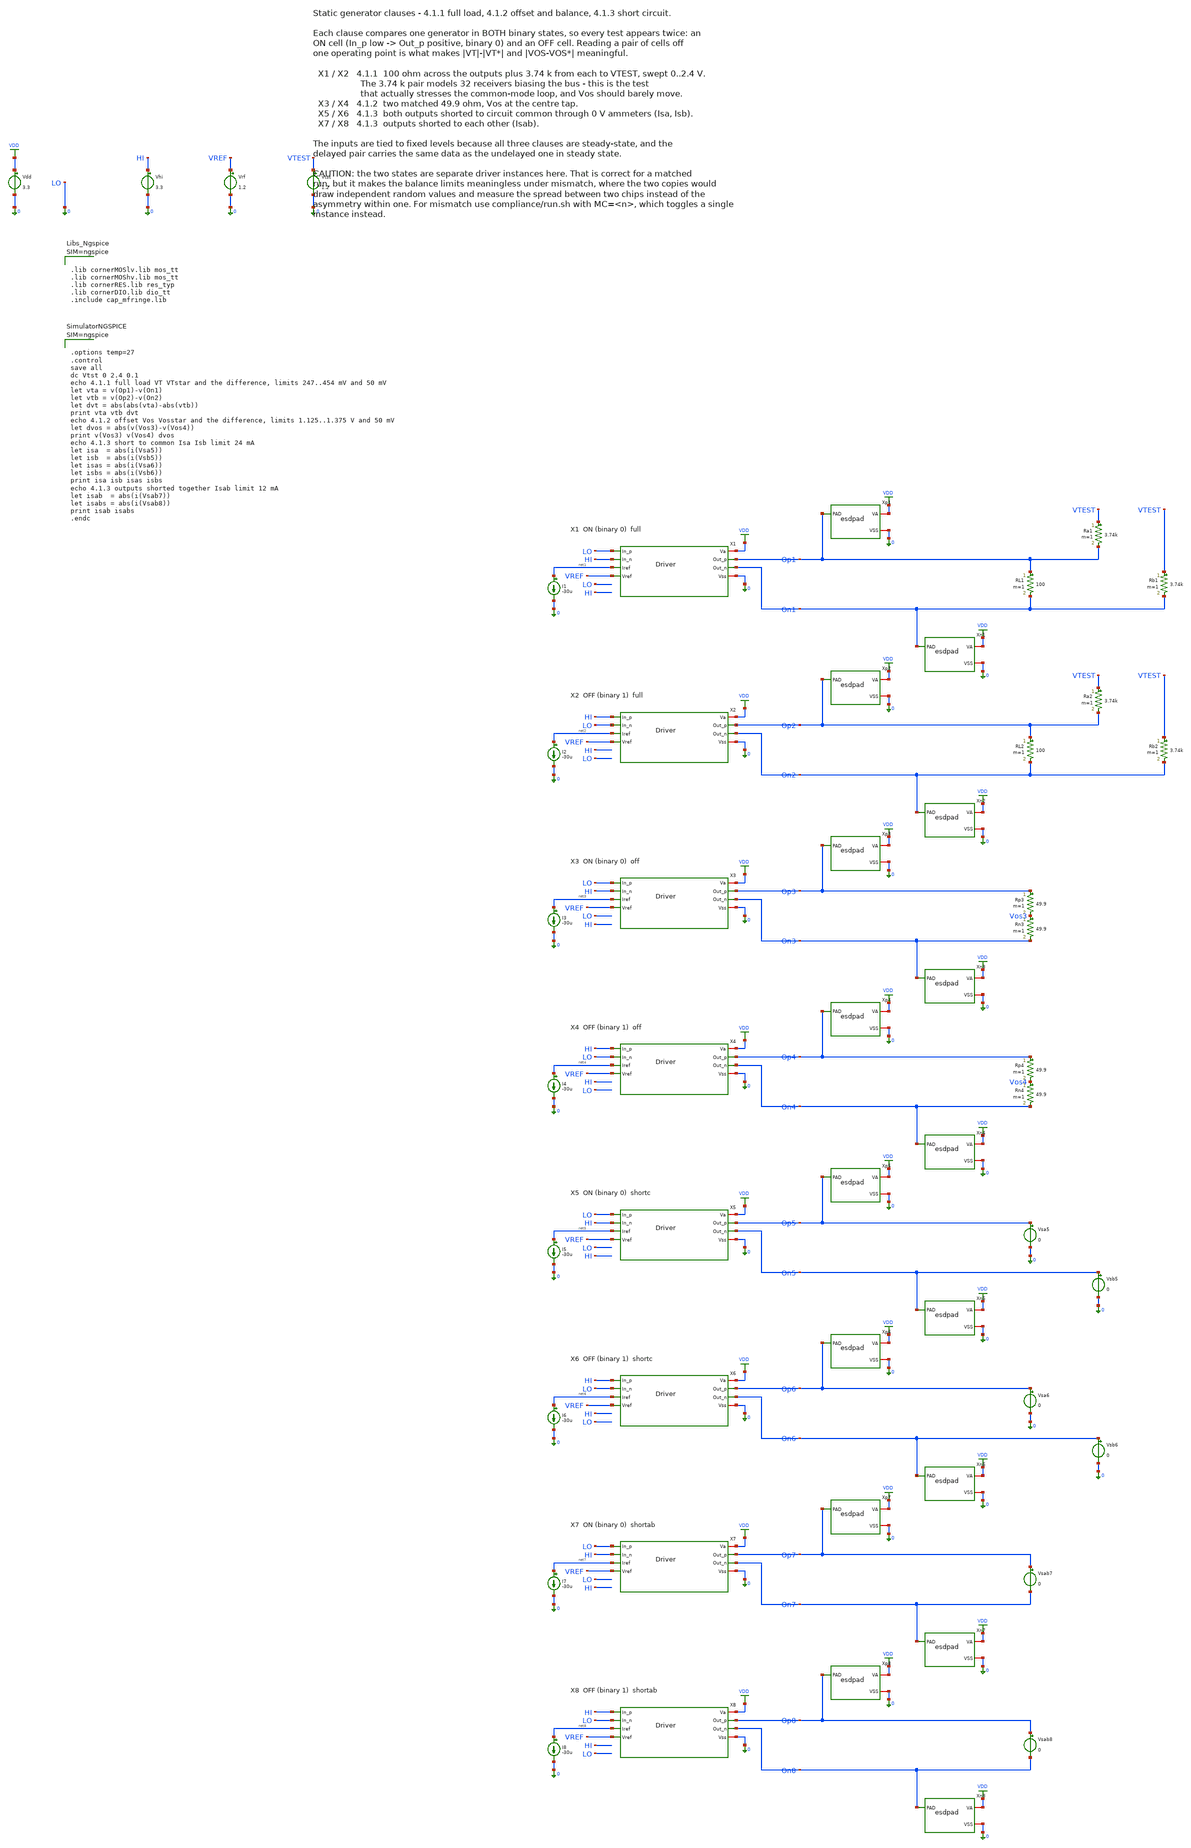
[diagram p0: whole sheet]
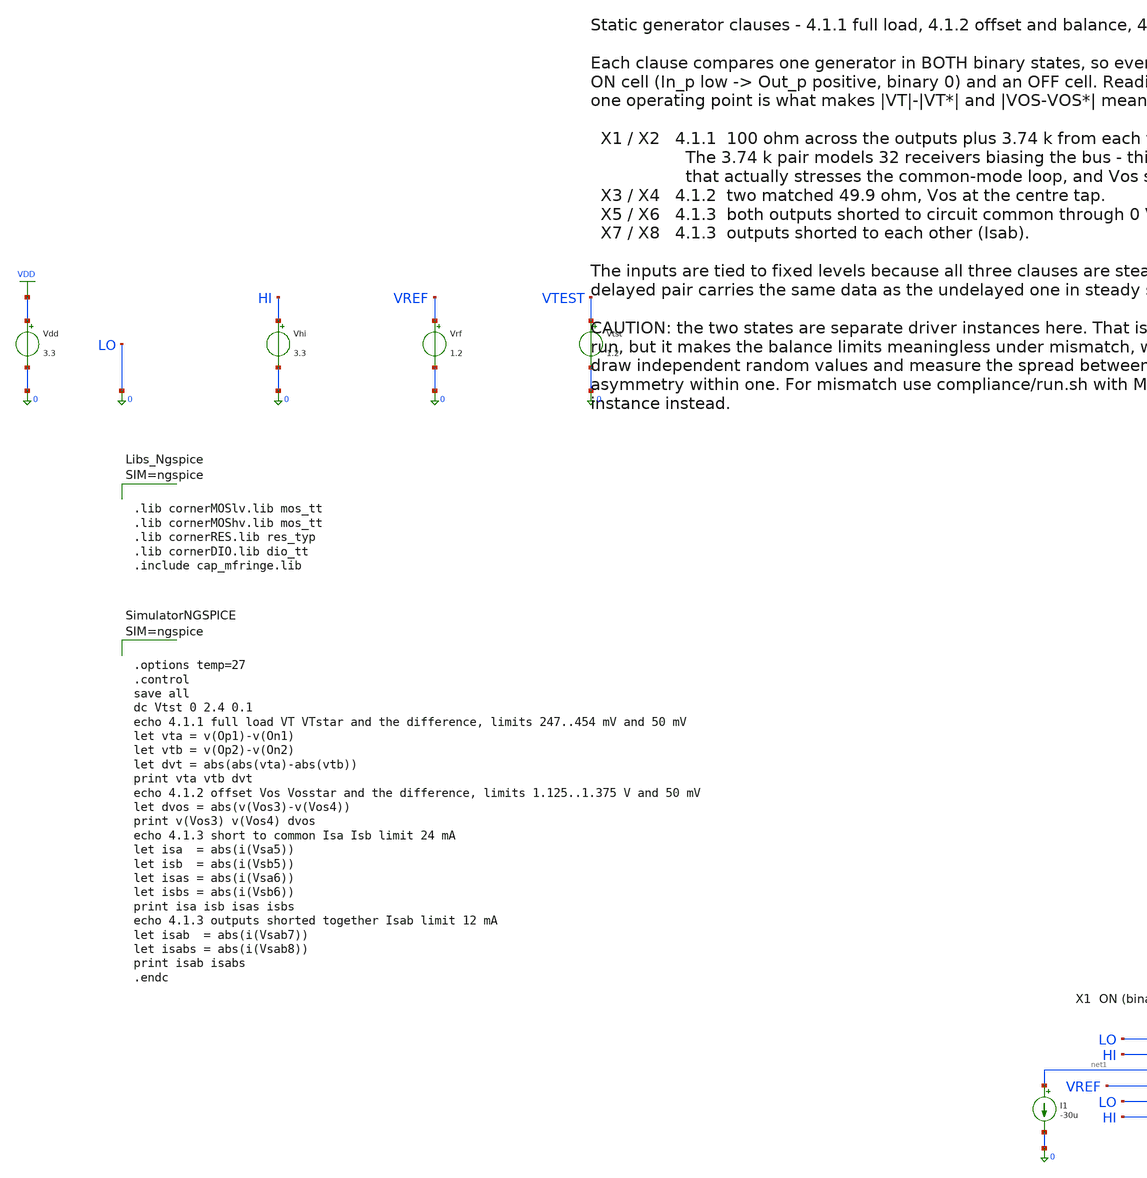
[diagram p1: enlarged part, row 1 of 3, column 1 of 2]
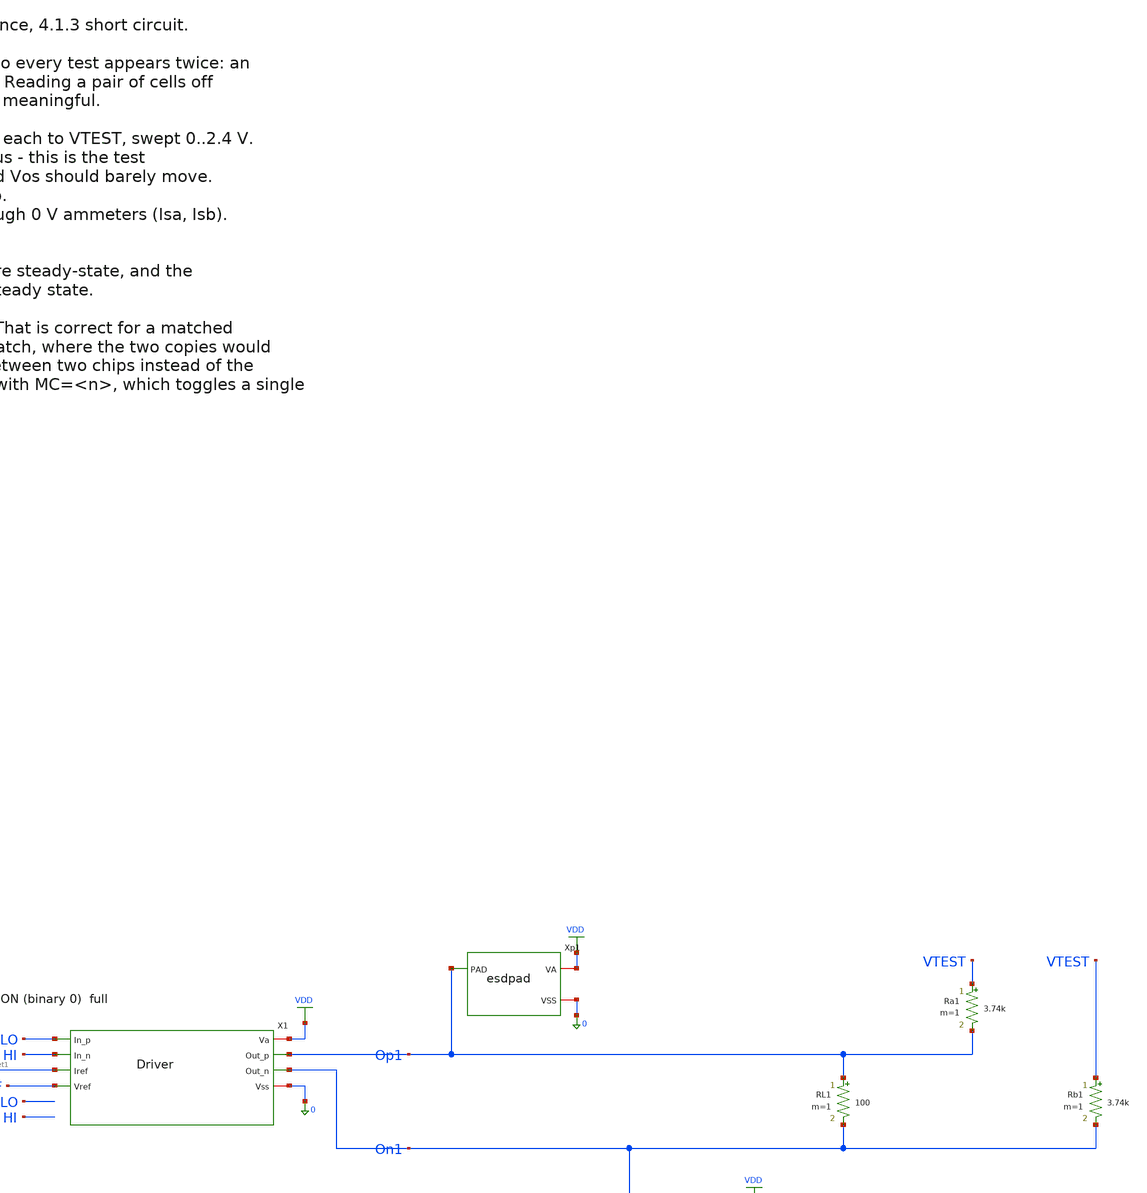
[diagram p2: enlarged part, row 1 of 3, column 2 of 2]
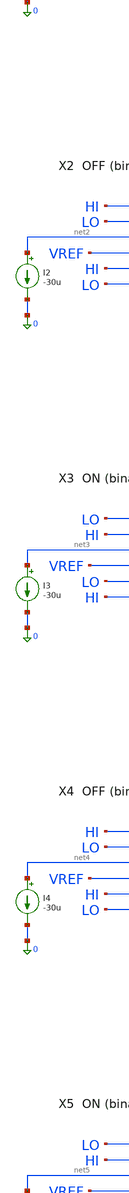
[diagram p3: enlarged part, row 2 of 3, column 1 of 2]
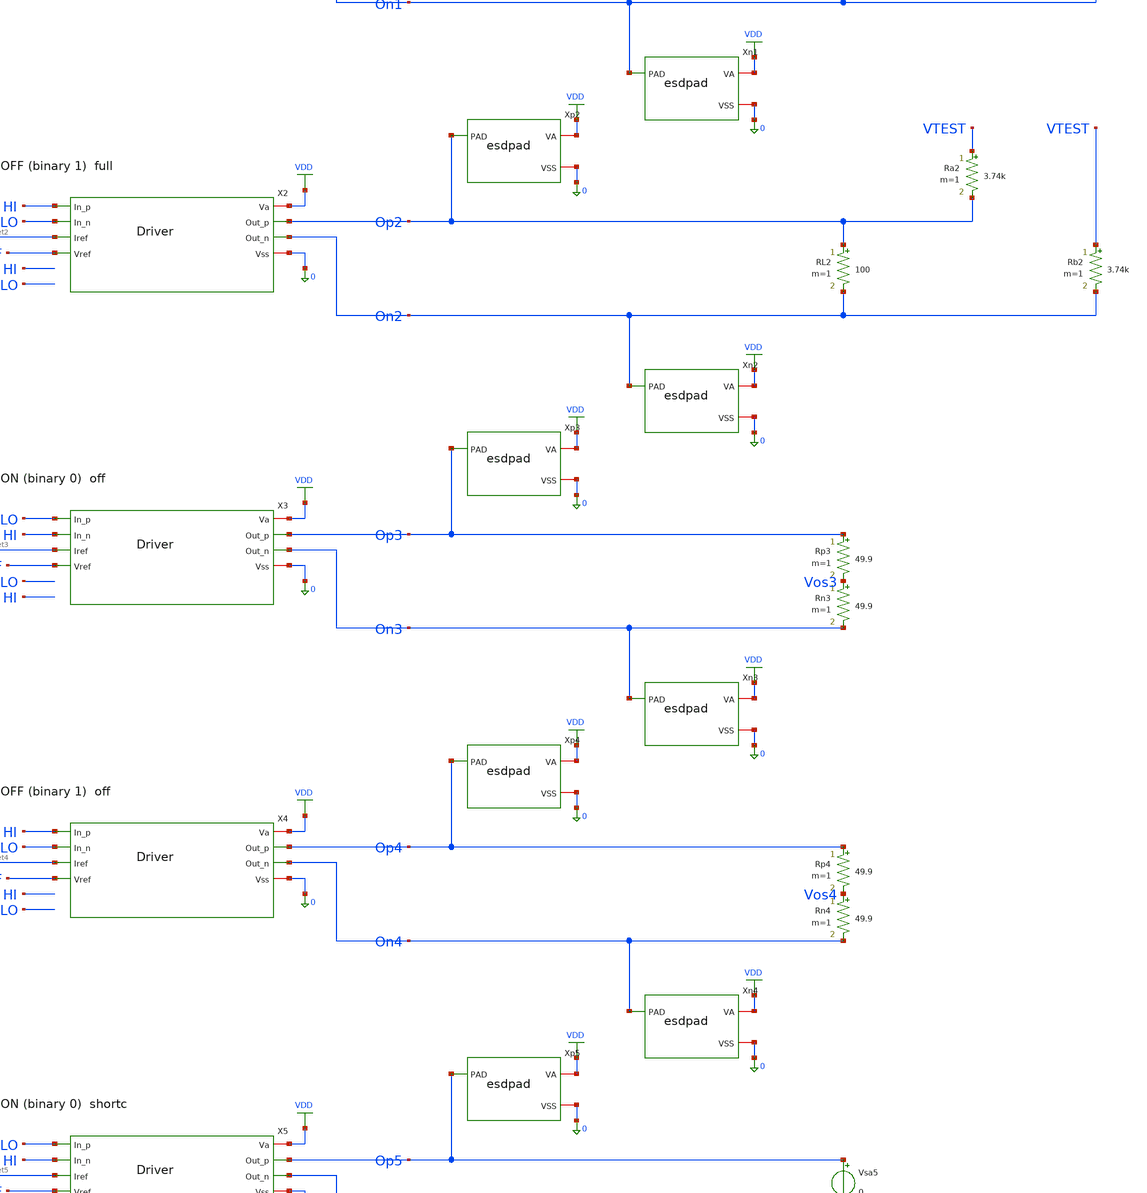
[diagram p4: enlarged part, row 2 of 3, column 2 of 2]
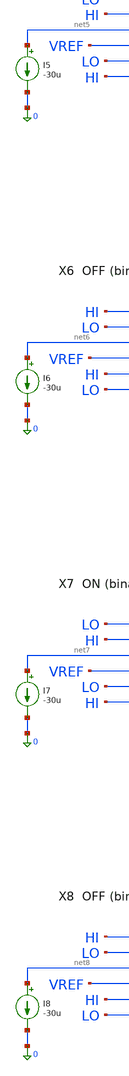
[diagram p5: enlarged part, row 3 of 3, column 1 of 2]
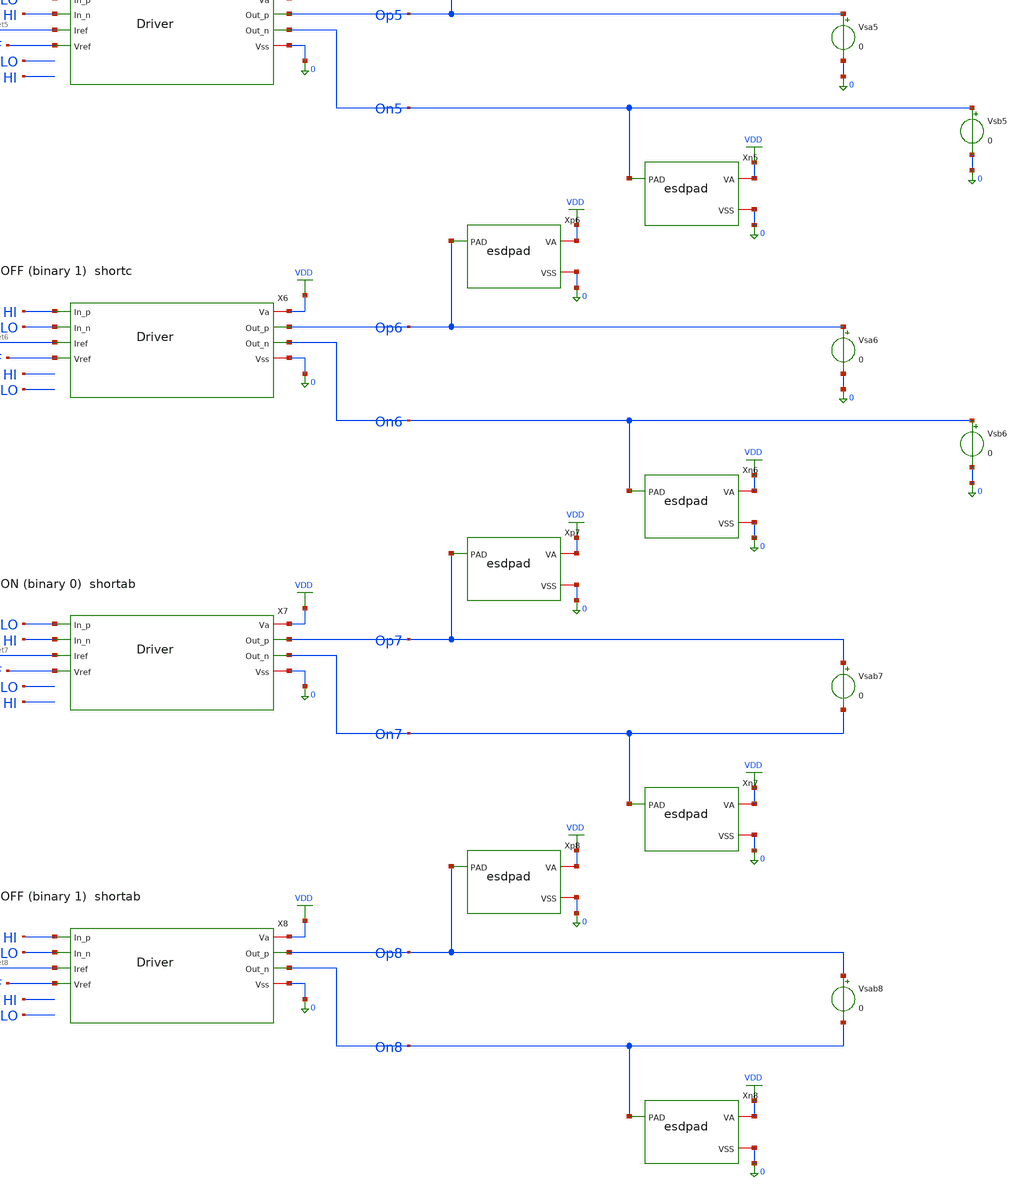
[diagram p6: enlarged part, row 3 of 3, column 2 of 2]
** sch_path: macros/lvds_tx/testbenches/xschem/tb_dc.sch
**.subckt tb_dc
Vdd VDD 0 3.3
Vhi HI 0 3.3
Vrf VREF 0 1.2
Vtst VTEST 0 1.2
X1 VDD Op1 LO HI net1 VREF On1 0 Driver
I1 net1 0 -30u
Xp1 Op1 VDD 0 esdpad
Xn1 On1 VDD 0 esdpad
RL1 Op1 On1 100 m=1
Ra1 VTEST Op1 3.74k m=1
Rb1 VTEST On1 3.74k m=1
X2 VDD Op2 HI LO net2 VREF On2 0 Driver
I2 net2 0 -30u
Xp2 Op2 VDD 0 esdpad
Xn2 On2 VDD 0 esdpad
RL2 Op2 On2 100 m=1
Ra2 VTEST Op2 3.74k m=1
Rb2 VTEST On2 3.74k m=1
X3 VDD Op3 LO HI net3 VREF On3 0 Driver
I3 net3 0 -30u
Xp3 Op3 VDD 0 esdpad
Xn3 On3 VDD 0 esdpad
Rp3 Op3 Vos3 49.9 m=1
Rn3 Vos3 On3 49.9 m=1
X4 VDD Op4 HI LO net4 VREF On4 0 Driver
I4 net4 0 -30u
Xp4 Op4 VDD 0 esdpad
Xn4 On4 VDD 0 esdpad
Rp4 Op4 Vos4 49.9 m=1
Rn4 Vos4 On4 49.9 m=1
X5 VDD Op5 LO HI net5 VREF On5 0 Driver
I5 net5 0 -30u
Xp5 Op5 VDD 0 esdpad
Xn5 On5 VDD 0 esdpad
Vsa5 Op5 0 0
.save i(vsa5)
Vsb5 On5 0 0
.save i(vsb5)
X6 VDD Op6 HI LO net6 VREF On6 0 Driver
I6 net6 0 -30u
Xp6 Op6 VDD 0 esdpad
Xn6 On6 VDD 0 esdpad
Vsa6 Op6 0 0
.save i(vsa6)
Vsb6 On6 0 0
.save i(vsb6)
X7 VDD Op7 LO HI net7 VREF On7 0 Driver
I7 net7 0 -30u
Xp7 Op7 VDD 0 esdpad
Xn7 On7 VDD 0 esdpad
Vsab7 Op7 On7 0
.save i(vsab7)
X8 VDD Op8 HI LO net8 VREF On8 0 Driver
I8 net8 0 -30u
Xp8 Op8 VDD 0 esdpad
Xn8 On8 VDD 0 esdpad
Vsab8 Op8 On8 0
.save i(vsab8)
**** begin user architecture code



.lib cornerMOSlv.lib mos_tt
.lib cornerMOShv.lib mos_tt
.lib cornerRES.lib res_typ
.lib cornerDIO.lib dio_tt
.include cap_mfringe.lib






.options temp=27
.control
save all
dc Vtst 0 2.4 0.1
echo 4.1.1 full load VT VTstar and the difference, limits 247..454 mV and 50 mV
let vta = v(Op1)-v(On1)
let vtb = v(Op2)-v(On2)
let dvt = abs(abs(vta)-abs(vtb))
print vta vtb dvt
echo 4.1.2 offset Vos Vosstar and the difference, limits 1.125..1.375 V and 50 mV
let dvos = abs(v(Vos3)-v(Vos4))
print v(Vos3) v(Vos4) dvos
echo 4.1.3 short to common Isa Isb limit 24 mA
let isa  = abs(i(Vsa5))
let isb  = abs(i(Vsb5))
let isas = abs(i(Vsa6))
let isbs = abs(i(Vsb6))
print isa isb isas isbs
echo 4.1.3 outputs shorted together Isab limit 12 mA
let isab  = abs(i(Vsab7))
let isabs = abs(i(Vsab8))
print isab isabs
.endc



**** end user architecture code
**.ends
.GLOBAL VDD
.end
